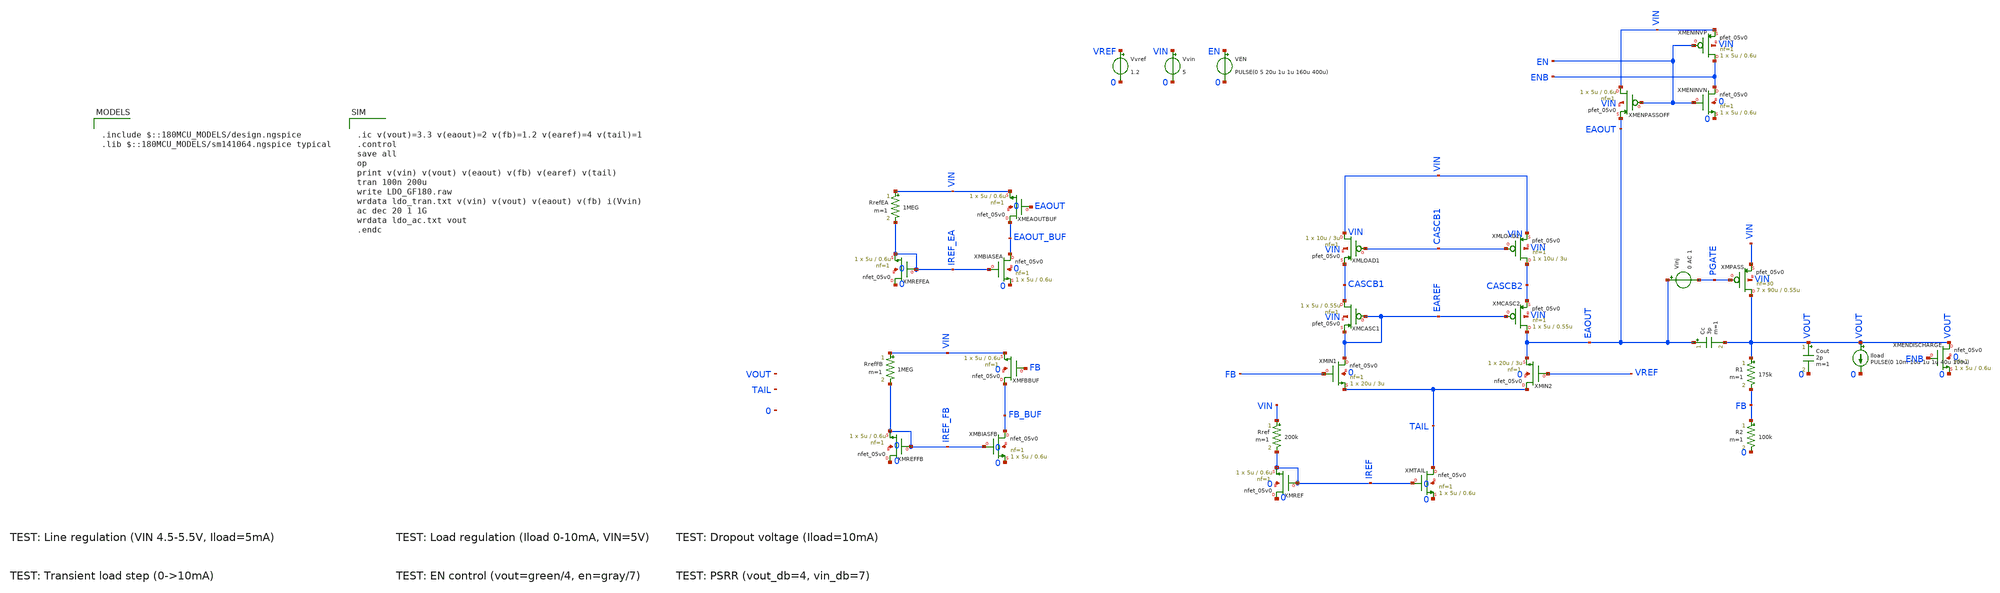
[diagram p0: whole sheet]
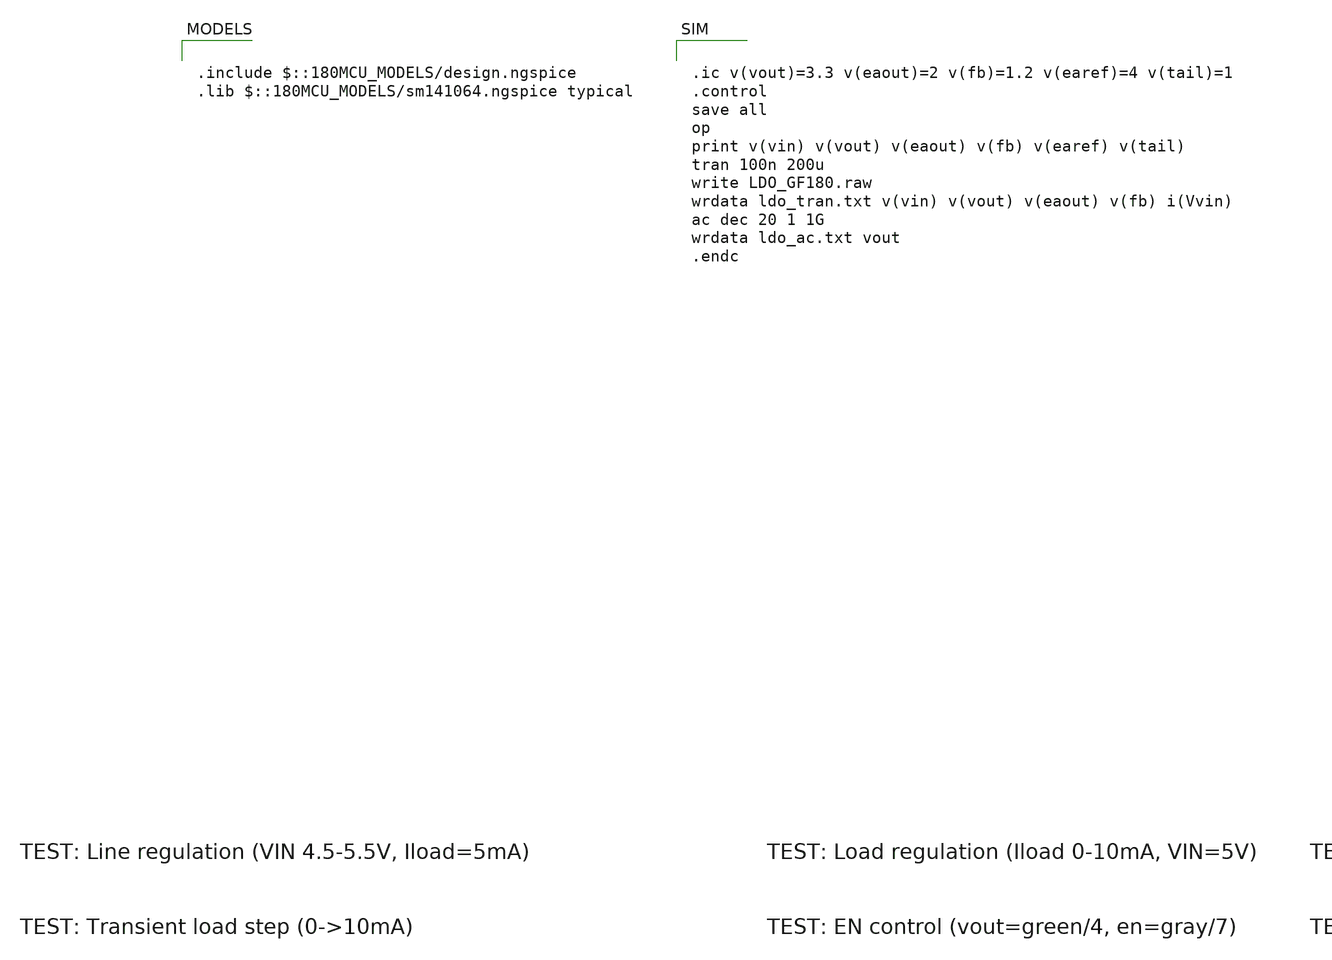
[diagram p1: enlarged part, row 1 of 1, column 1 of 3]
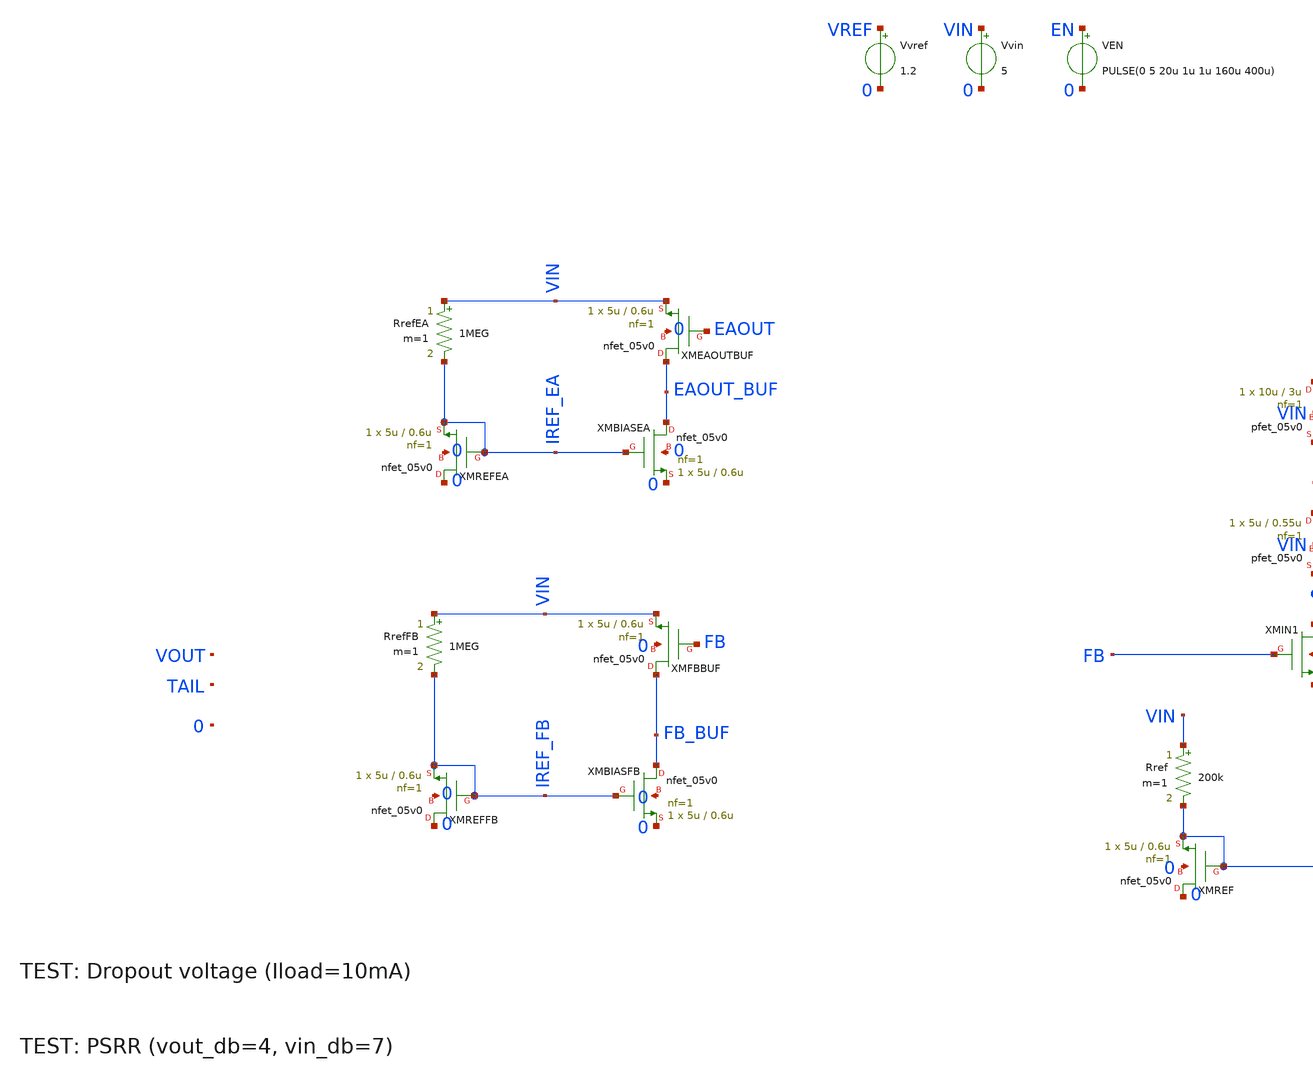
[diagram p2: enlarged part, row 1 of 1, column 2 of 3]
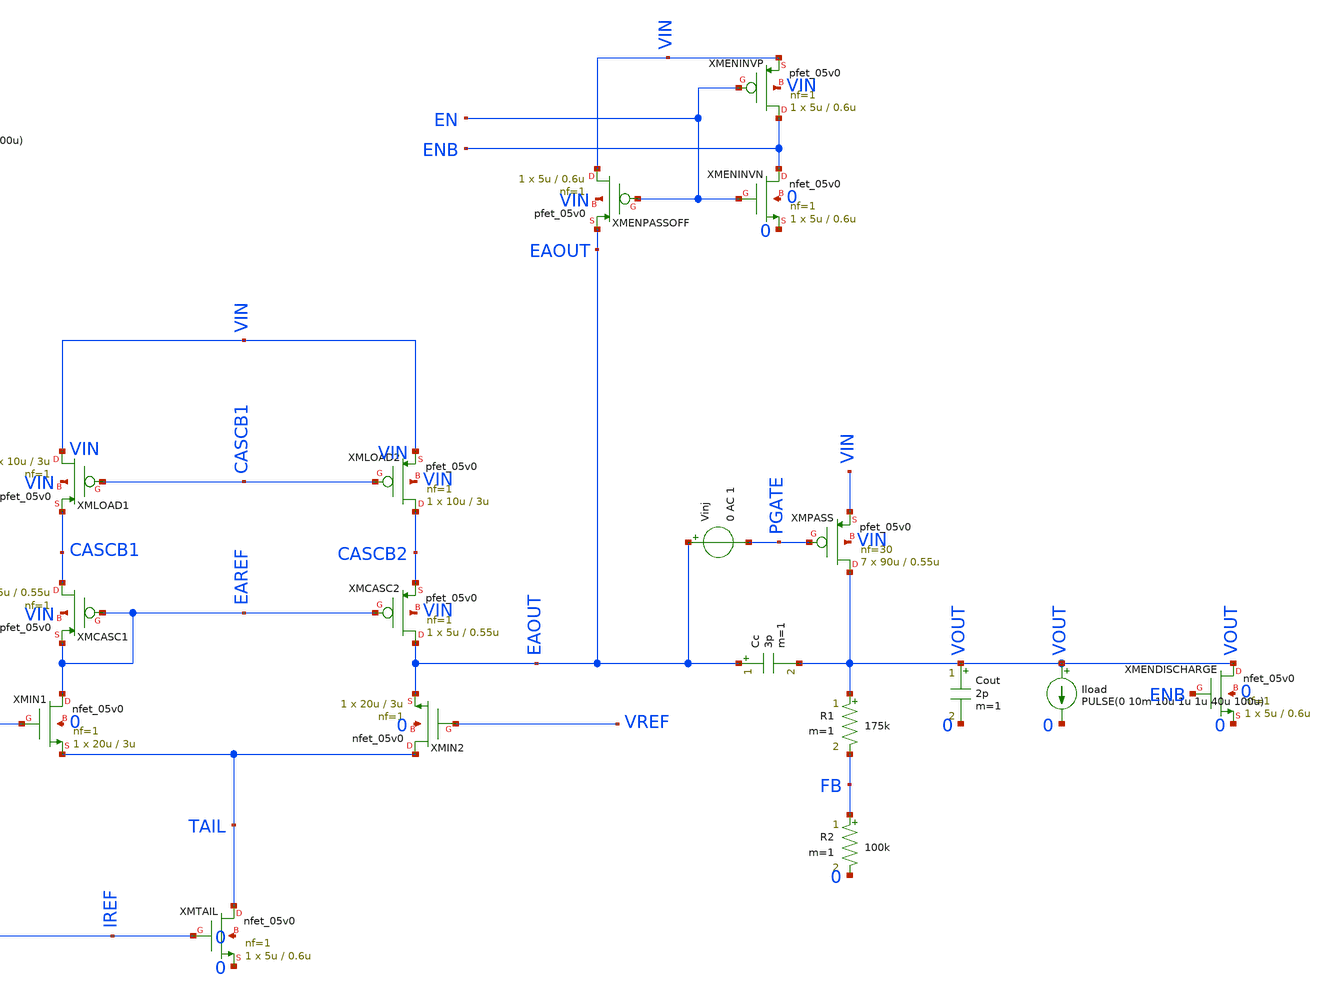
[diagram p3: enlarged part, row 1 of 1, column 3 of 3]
** sch_path: LDO_GF180_MAIN.sch
**.subckt LDO_GF180_MAIN
Vvin VIN 0 5
Vvref VREF 0 1.2
Rref VIN IREF 200k m=1
XMREF 0 IREF IREF 0 nfet_05v0 L=0.6u W=5u nf=1 ad='int((nf+1)/2) * W/nf * 0.18u' as='int((nf+2)/2) * W/nf * 0.18u'
+ pd='2*int((nf+1)/2) * (W/nf + 0.18u)' ps='2*int((nf+2)/2) * (W/nf + 0.18u)' nrd='0.18u / W' nrs='0.18u / W'
+ sa=0 sb=0 sd=0 m=1
XMTAIL TAIL IREF 0 0 nfet_05v0 L=0.6u W=5u nf=1 ad='int((nf+1)/2) * W/nf * 0.18u' as='int((nf+2)/2) * W/nf * 0.18u'
+ pd='2*int((nf+1)/2) * (W/nf + 0.18u)' ps='2*int((nf+2)/2) * (W/nf + 0.18u)' nrd='0.18u / W' nrs='0.18u / W'
+ sa=0 sb=0 sd=0 m=1
VEN EN 0 PULSE(0 5 20u 1u 1u 160u 400u)
XMENINVP ENB EN VIN VIN pfet_05v0 L=0.6u W=5u nf=1 ad='int((nf+1)/2) * W/nf * 0.18u' as='int((nf+2)/2) * W/nf * 0.18u'
+ pd='2*int((nf+1)/2) * (W/nf + 0.18u)' ps='2*int((nf+2)/2) * (W/nf + 0.18u)' nrd='0.18u / W' nrs='0.18u / W'
+ sa=0 sb=0 sd=0 m=1
XMENINVN ENB EN 0 0 nfet_05v0 L=0.6u W=5u nf=1 ad='int((nf+1)/2) * W/nf * 0.18u' as='int((nf+2)/2) * W/nf * 0.18u'
+ pd='2*int((nf+1)/2) * (W/nf + 0.18u)' ps='2*int((nf+2)/2) * (W/nf + 0.18u)' nrd='0.18u / W' nrs='0.18u / W'
+ sa=0 sb=0 sd=0 m=1
XMENPASSOFF VIN EN EAOUT VIN pfet_05v0 L=0.6u W=5u nf=1 ad='int((nf+1)/2) * W/nf * 0.18u' as='int((nf+2)/2) * W/nf * 0.18u'
+ pd='2*int((nf+1)/2) * (W/nf + 0.18u)' ps='2*int((nf+2)/2) * (W/nf + 0.18u)' nrd='0.18u / W' nrs='0.18u / W'
+ sa=0 sb=0 sd=0 m=1
XMENDISCHARGE VOUT ENB 0 0 nfet_05v0 L=0.6u W=5u nf=1 ad='int((nf+1)/2) * W/nf * 0.18u' as='int((nf+2)/2) * W/nf * 0.18u'
+ pd='2*int((nf+1)/2) * (W/nf + 0.18u)' ps='2*int((nf+2)/2) * (W/nf + 0.18u)' nrd='0.18u / W' nrs='0.18u / W'
+ sa=0 sb=0 sd=0 m=1
RrefFB VIN IREF_FB 1MEG m=1
XMREFFB 0 IREF_FB IREF_FB 0 nfet_05v0 L=0.6u W=5u nf=1 ad='int((nf+1)/2) * W/nf * 0.18u' as='int((nf+2)/2) * W/nf * 0.18u'
+ pd='2*int((nf+1)/2) * (W/nf + 0.18u)' ps='2*int((nf+2)/2) * (W/nf + 0.18u)' nrd='0.18u / W' nrs='0.18u / W'
+ sa=0 sb=0 sd=0 m=1
XMFBBUF FB_BUF FB VIN 0 nfet_05v0 L=0.6u W=5u nf=1 ad='int((nf+1)/2) * W/nf * 0.18u' as='int((nf+2)/2) * W/nf * 0.18u'
+ pd='2*int((nf+1)/2) * (W/nf + 0.18u)' ps='2*int((nf+2)/2) * (W/nf + 0.18u)' nrd='0.18u / W' nrs='0.18u / W'
+ sa=0 sb=0 sd=0 m=1
XMBIASFB FB_BUF IREF_FB 0 0 nfet_05v0 L=0.6u W=5u nf=1 ad='int((nf+1)/2) * W/nf * 0.18u' as='int((nf+2)/2) * W/nf * 0.18u'
+ pd='2*int((nf+1)/2) * (W/nf + 0.18u)' ps='2*int((nf+2)/2) * (W/nf + 0.18u)' nrd='0.18u / W' nrs='0.18u / W'
+ sa=0 sb=0 sd=0 m=1
RrefEA VIN IREF_EA 1MEG m=1
XMREFEA 0 IREF_EA IREF_EA 0 nfet_05v0 L=0.6u W=5u nf=1 ad='int((nf+1)/2) * W/nf * 0.18u' as='int((nf+2)/2) * W/nf * 0.18u'
+ pd='2*int((nf+1)/2) * (W/nf + 0.18u)' ps='2*int((nf+2)/2) * (W/nf + 0.18u)' nrd='0.18u / W' nrs='0.18u / W'
+ sa=0 sb=0 sd=0 m=1
XMEAOUTBUF EAOUT_BUF EAOUT VIN 0 nfet_05v0 L=0.6u W=5u nf=1 ad='int((nf+1)/2) * W/nf * 0.18u' as='int((nf+2)/2) * W/nf * 0.18u'
+ pd='2*int((nf+1)/2) * (W/nf + 0.18u)' ps='2*int((nf+2)/2) * (W/nf + 0.18u)' nrd='0.18u / W' nrs='0.18u / W'
+ sa=0 sb=0 sd=0 m=1
XMBIASEA EAOUT_BUF IREF_EA 0 0 nfet_05v0 L=0.6u W=5u nf=1 ad='int((nf+1)/2) * W/nf * 0.18u' as='int((nf+2)/2) * W/nf * 0.18u'
+ pd='2*int((nf+1)/2) * (W/nf + 0.18u)' ps='2*int((nf+2)/2) * (W/nf + 0.18u)' nrd='0.18u / W' nrs='0.18u / W'
+ sa=0 sb=0 sd=0 m=1
XMIN1 EAREF FB TAIL 0 nfet_05v0 L=3u W=20u nf=1 ad='int((nf+1)/2) * W/nf * 0.18u' as='int((nf+2)/2) * W/nf * 0.18u'
+ pd='2*int((nf+1)/2) * (W/nf + 0.18u)' ps='2*int((nf+2)/2) * (W/nf + 0.18u)' nrd='0.18u / W' nrs='0.18u / W'
+ sa=0 sb=0 sd=0 m=1
XMIN2 TAIL VREF EAOUT 0 nfet_05v0 L=3u W=20u nf=1 ad='int((nf+1)/2) * W/nf * 0.18u' as='int((nf+2)/2) * W/nf * 0.18u'
+ pd='2*int((nf+1)/2) * (W/nf + 0.18u)' ps='2*int((nf+2)/2) * (W/nf + 0.18u)' nrd='0.18u / W' nrs='0.18u / W'
+ sa=0 sb=0 sd=0 m=1
XMLOAD1 VIN CASCB1 CASCB1 VIN pfet_05v0 L=3u W=10u nf=1 ad='int((nf+1)/2) * W/nf * 0.18u' as='int((nf+2)/2) * W/nf * 0.18u'
+ pd='2*int((nf+1)/2) * (W/nf + 0.18u)' ps='2*int((nf+2)/2) * (W/nf + 0.18u)' nrd='0.18u / W' nrs='0.18u / W'
+ sa=0 sb=0 sd=0 m=1
XMLOAD2 CASCB2 CASCB1 VIN VIN pfet_05v0 L=3u W=10u nf=1 ad='int((nf+1)/2) * W/nf * 0.18u' as='int((nf+2)/2) * W/nf * 0.18u'
+ pd='2*int((nf+1)/2) * (W/nf + 0.18u)' ps='2*int((nf+2)/2) * (W/nf + 0.18u)' nrd='0.18u / W' nrs='0.18u / W'
+ sa=0 sb=0 sd=0 m=1
XMPASS VOUT PGATE VIN VIN pfet_05v0 L=0.55u W=90u nf=30 ad='int((nf+1)/2) * W/nf * 0.18u' as='int((nf+2)/2) * W/nf * 0.18u'
+ pd='2*int((nf+1)/2) * (W/nf + 0.18u)' ps='2*int((nf+2)/2) * (W/nf + 0.18u)' nrd='0.18u / W' nrs='0.18u / W'
+ sa=0 sb=0 sd=0 m=7
Vinj EAOUT PGATE 0 AC 1
Cc EAOUT VOUT 3p m=1
R1 VOUT FB 175k m=1
R2 FB 0 100k m=1
Cout VOUT 0 2p m=1
Iload VOUT 0 PULSE(0 10m 10u 1u 1u 40u 100u)
XMCASC1 CASCB1 EAREF EAREF VIN pfet_05v0 L=0.55u W=5u nf=1 ad='int((nf+1)/2) * W/nf * 0.18u' as='int((nf+2)/2) * W/nf * 0.18u'
+ pd='2*int((nf+1)/2) * (W/nf + 0.18u)' ps='2*int((nf+2)/2) * (W/nf + 0.18u)' nrd='0.18u / W' nrs='0.18u / W'
+ sa=0 sb=0 sd=0 m=1
XMCASC2 EAOUT EAREF CASCB2 VIN pfet_05v0 L=0.55u W=5u nf=1 ad='int((nf+1)/2) * W/nf * 0.18u' as='int((nf+2)/2) * W/nf * 0.18u'
+ pd='2*int((nf+1)/2) * (W/nf + 0.18u)' ps='2*int((nf+2)/2) * (W/nf + 0.18u)' nrd='0.18u / W' nrs='0.18u / W'
+ sa=0 sb=0 sd=0 m=1
**** begin user architecture code

.include $::180MCU_MODELS/design.ngspice
.lib $::180MCU_MODELS/sm141064.ngspice typical



.ic v(vout)=3.3 v(eaout)=2 v(fb)=1.2 v(earef)=4 v(tail)=1
.control
save all
op
print v(vin) v(vout) v(eaout) v(fb) v(earef) v(tail)
tran 100n 200u
write LDO_GF180.raw
wrdata ldo_tran.txt v(vin) v(vout) v(eaout) v(fb) i(Vvin)
ac dec 20 1 1G
wrdata ldo_ac.txt vout
.endc


**** end user architecture code
**.ends
.end
